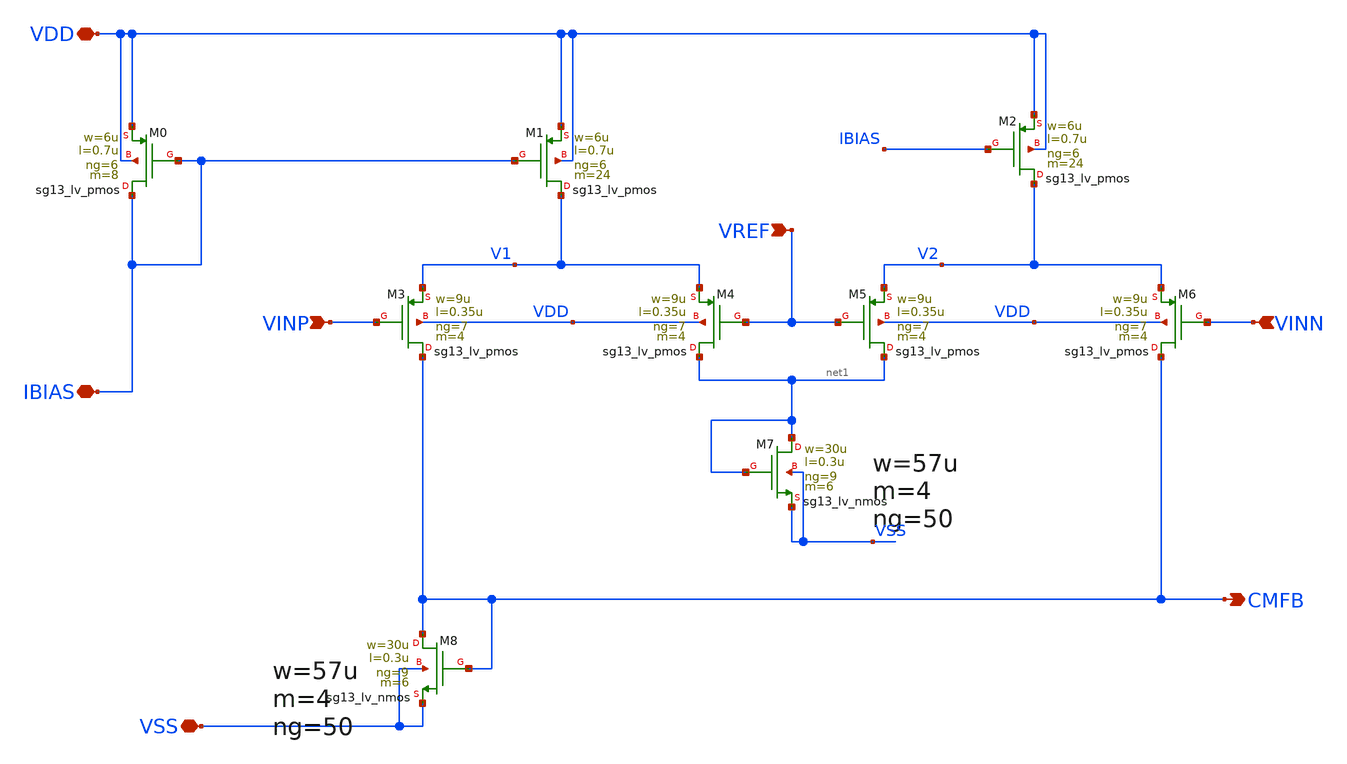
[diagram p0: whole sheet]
** sch_path: HPAmplifier/Differential_OTA_Telescopic_IHP/OTA_Telescopic_CMFB2.sch
**.subckt OTA_Telescopic_CMFB2 VDD VSS CMFB VREF IBIAS VINP VINN
*.iopin VDD
*.iopin VSS
*.opin CMFB
*.ipin VREF
*.iopin IBIAS
*.ipin VINP
*.ipin VINN
XM0 IBIAS IBIAS VDD VDD sg13_lv_pmos w=6u l=0.7u ng=6 m=8 mm_ok=1
XM1 V1 IBIAS VDD VDD sg13_lv_pmos w=6u l=0.7u ng=6 m=24 mm_ok=1
XM2 V2 IBIAS VDD VDD sg13_lv_pmos w=6u l=0.7u ng=6 m=24 mm_ok=1
XM3 CMFB VINP V1 VDD sg13_lv_pmos w=9u l=0.35u ng=7 m=4 mm_ok=1
XM4 net1 VREF V1 VDD sg13_lv_pmos w=9u l=0.35u ng=7 m=4 mm_ok=1
XM5 net1 VREF V2 VDD sg13_lv_pmos w=9u l=0.35u ng=7 m=4 mm_ok=1
XM6 CMFB VINN V2 VDD sg13_lv_pmos w=9u l=0.35u ng=7 m=4 mm_ok=1
XM7 net1 net1 VSS VSS sg13_lv_nmos w=30u l=0.3u ng=9 m=6 mm_ok=1
XM8 CMFB CMFB VSS VSS sg13_lv_nmos w=30u l=0.3u ng=9 m=6 mm_ok=1
**.ends
.end
